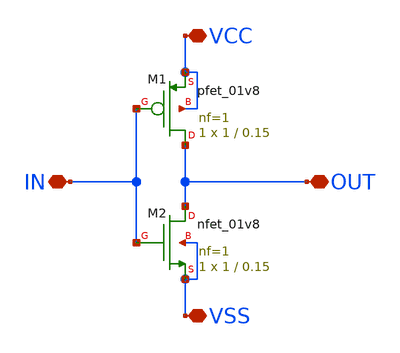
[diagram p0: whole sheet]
** sch_path: inverter.sch
**.subckt inverter VCC VSS OUT IN
*.iopin VCC
*.iopin VSS
*.iopin OUT
*.iopin IN
XM2 OUT IN VSS VSS sky130_fd_pr__nfet_01v8 L=0.15 W=1 nf=1 ad='int((1 + 1)/2) * 1 / 1 * 0.29' as='int((1 + 2)/2) * 1 / 1 * 0.29'
+ pd='2*int((1 + 1)/2) * (1 / 1 + 0.29)' ps='2*int((1 + 2)/2) * (1 / 1 + 0.29)' nrd='0.29 / 1 ' nrs='0.29 / 1 '
+ sa=0 sb=0 sd=0 mult=1 m=1
XM1 OUT IN VCC VCC sky130_fd_pr__pfet_01v8 L=0.15 W=1 nf=1 ad='int((1 + 1)/2) * 1 / 1 * 0.29' as='int((1 + 2)/2) * 1 / 1 * 0.29'
+ pd='2*int((1 + 1)/2) * (1 / 1 + 0.29)' ps='2*int((1 + 2)/2) * (1 / 1 + 0.29)' nrd='0.29 / 1 ' nrs='0.29 / 1 '
+ sa=0 sb=0 sd=0 mult=1 m=1
**.ends
.end
